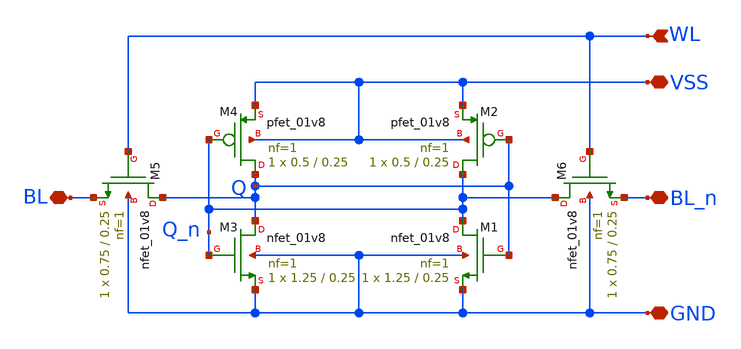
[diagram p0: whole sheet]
** sch_path: SRAM_cell.sch
**.subckt SRAM_cell WL BL BL_n VSS GND
*.ipin WL
*.iopin BL
*.iopin BL_n
*.iopin VSS
*.iopin GND
XM1 Q_n Q GND GND sky130_fd_pr__nfet_01v8 L=0.25 W=1.25 nf=1 ad='int((nf+1)/2) * W/nf * 0.29' as='int((nf+2)/2) * W/nf * 0.29'
+ pd='2*int((nf+1)/2) * (W/nf + 0.29)' ps='2*int((nf+2)/2) * (W/nf + 0.29)' nrd='0.29 / W' nrs='0.29 / W'
+ sa=0 sb=0 sd=0 mult=1 m=1
XM2 Q_n Q VSS VSS sky130_fd_pr__pfet_01v8 L=0.25 W=0.5 nf=1 ad='int((nf+1)/2) * W/nf * 0.29' as='int((nf+2)/2) * W/nf * 0.29'
+ pd='2*int((nf+1)/2) * (W/nf + 0.29)' ps='2*int((nf+2)/2) * (W/nf + 0.29)' nrd='0.29 / W' nrs='0.29 / W'
+ sa=0 sb=0 sd=0 mult=1 m=1
XM3 Q Q_n GND GND sky130_fd_pr__nfet_01v8 L=0.25 W=1.25 nf=1 ad='int((nf+1)/2) * W/nf * 0.29' as='int((nf+2)/2) * W/nf * 0.29'
+ pd='2*int((nf+1)/2) * (W/nf + 0.29)' ps='2*int((nf+2)/2) * (W/nf + 0.29)' nrd='0.29 / W' nrs='0.29 / W'
+ sa=0 sb=0 sd=0 mult=1 m=1
XM4 Q Q_n VSS VSS sky130_fd_pr__pfet_01v8 L=0.25 W=0.5 nf=1 ad='int((nf+1)/2) * W/nf * 0.29' as='int((nf+2)/2) * W/nf * 0.29'
+ pd='2*int((nf+1)/2) * (W/nf + 0.29)' ps='2*int((nf+2)/2) * (W/nf + 0.29)' nrd='0.29 / W' nrs='0.29 / W'
+ sa=0 sb=0 sd=0 mult=1 m=1
XM5 Q WL BL GND sky130_fd_pr__nfet_01v8 L=0.25 W=0.75 nf=1 ad='int((nf+1)/2) * W/nf * 0.29' as='int((nf+2)/2) * W/nf * 0.29'
+ pd='2*int((nf+1)/2) * (W/nf + 0.29)' ps='2*int((nf+2)/2) * (W/nf + 0.29)' nrd='0.29 / W' nrs='0.29 / W'
+ sa=0 sb=0 sd=0 mult=1 m=1
XM6 Q_n WL BL_n GND sky130_fd_pr__nfet_01v8 L=0.25 W=0.75 nf=1 ad='int((nf+1)/2) * W/nf * 0.29' as='int((nf+2)/2) * W/nf * 0.29'
+ pd='2*int((nf+1)/2) * (W/nf + 0.29)' ps='2*int((nf+2)/2) * (W/nf + 0.29)' nrd='0.29 / W' nrs='0.29 / W'
+ sa=0 sb=0 sd=0 mult=1 m=1
**.ends
.end
